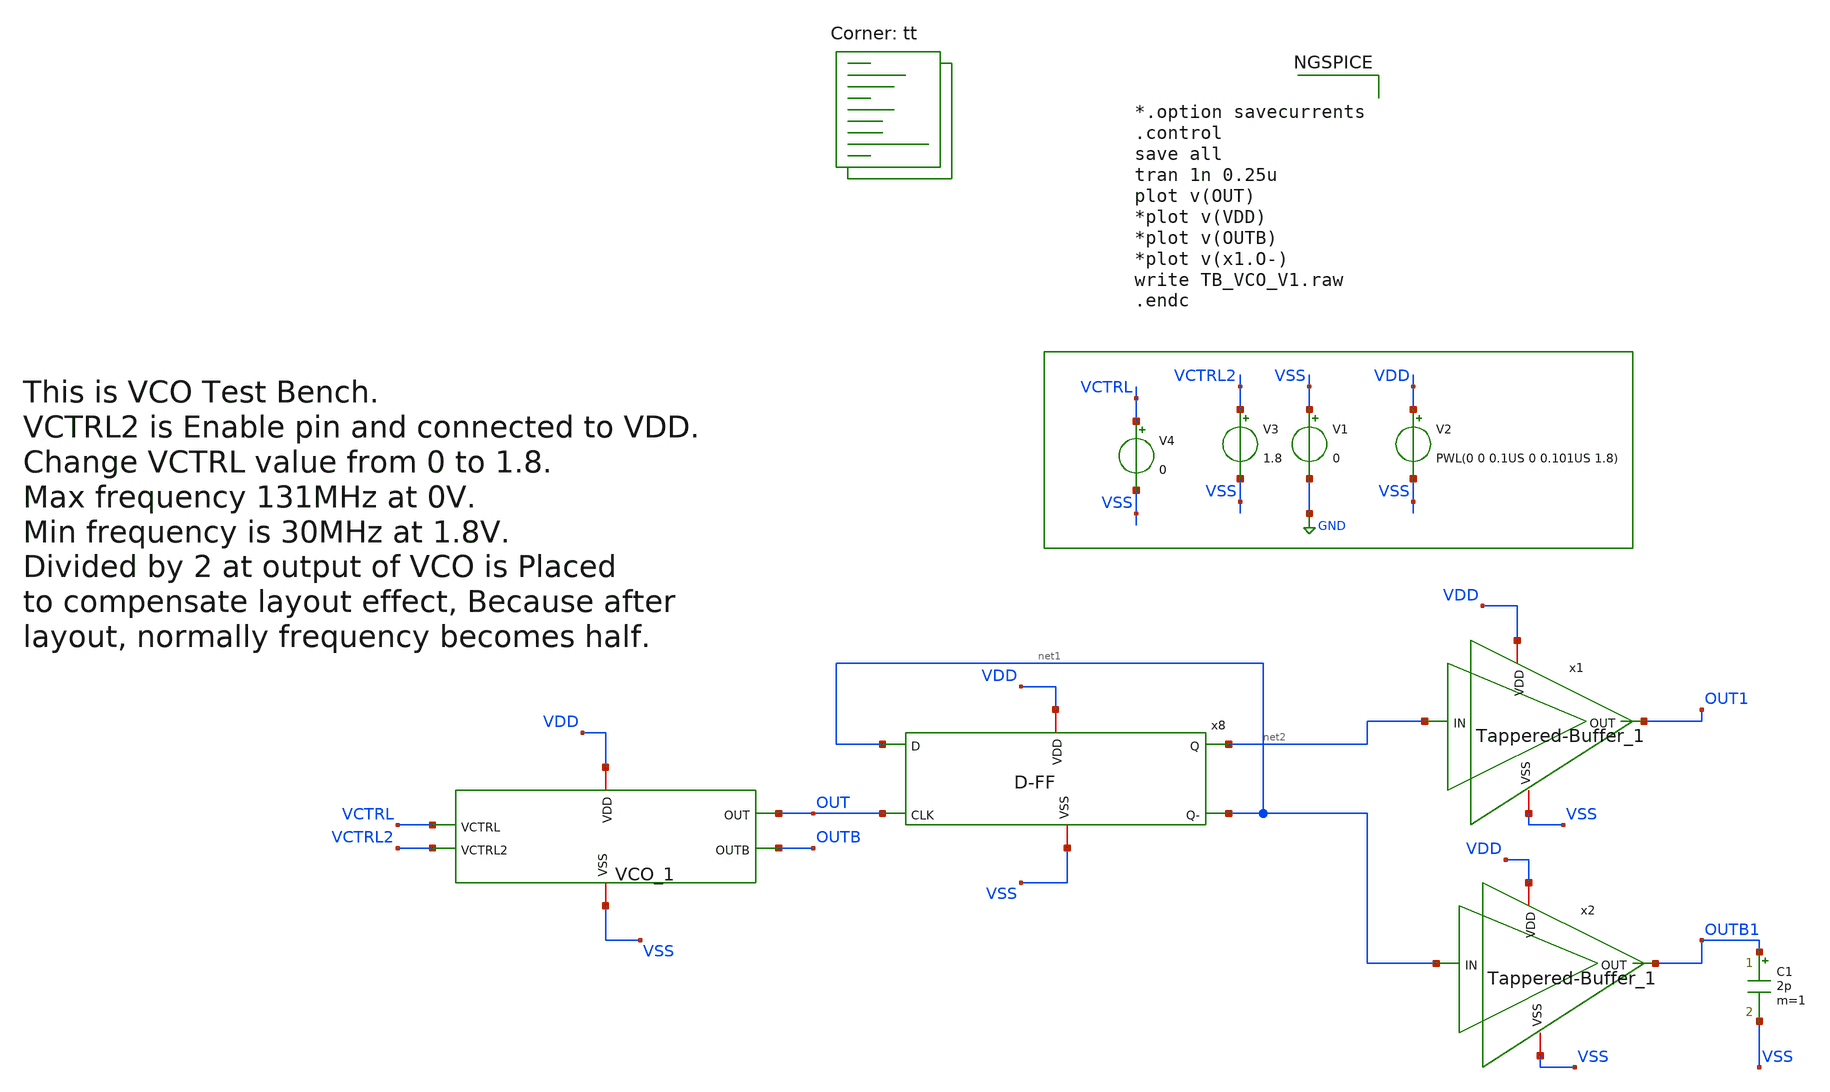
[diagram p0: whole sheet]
** sch_path: Xschem/PLL_TOP_Schematics/TB_VCO_V1.sch
**.subckt TB_VCO_V1
V1 VSS GND 0
V2 VDD VSS PWL(0 0 0.1US 0 0.101US 1.8)
V3 VCTRL2 VSS 1.8
V4 VCTRL VSS 0
x7 VDD VSS VCTRL VCTRL2 OUT OUTB VCO_1
x8 VDD VSS OUT net1 net2 net1 D-FF
x1 VSS VDD OUT1 net2 Tappered-Buffer_1
x2 VSS VDD OUTB1 net1 Tappered-Buffer_1
C1 OUTB1 VSS 2p m=1
**** begin user architecture code


*.option savecurrents
.control
save all
tran 1n 0.25u
plot v(OUT)
*plot v(VDD)
*plot v(OUTB)
*plot v(x1.O-)
write TB_VCO_V1.raw
.endc


.lib $::SKYWATER_MODELS/sky130.lib.spice tt
**** end user architecture code
**.ends
.GLOBAL GND
.end
